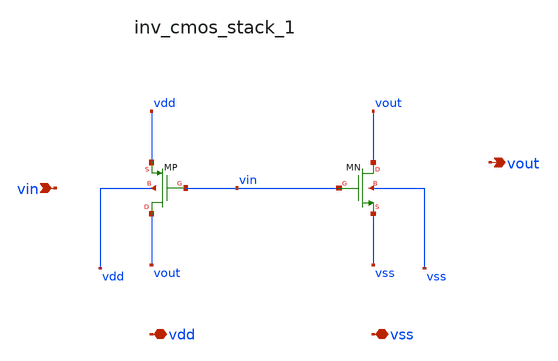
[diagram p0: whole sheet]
** sch_path: analog-db/raw/adc_001_inv1b/hier/blocks/inv_cmos_stack_1.sch
**.subckt inv_cmos_stack_1 vin vdd vss vout
*.ipin vin
*.iopin vdd
*.iopin vss
*.opin vout
XMN vout vin vss vss sg13_lv_nmos w=x_dut_xmn_w l=x_dut_xmn_l ng=1 m=x_dut_xmn_m
XMP vout vin vdd vdd sg13_lv_pmos w=x_dut_xmp_w l=x_dut_xmp_l ng=1 m=x_dut_xmp_m
**.ends
.end
